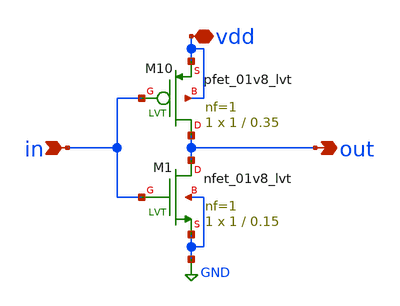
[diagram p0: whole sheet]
** sch_path: designs/subcells/core_not/not.sch
**.subckt not in out vdd
*.ipin in
*.opin out
*.iopin vdd
XM10 out in vdd vdd sky130_fd_pr__pfet_01v8_lvt L=0.35 W=1 nf=1 ad='int((1 + 1)/2) * 1 / 1 * 0.29' as='int((1 + 2)/2) * 1 / 1 * 0.29'
+ pd='2*int((1 + 1)/2) * (1 / 1 + 0.29)' ps='2*int((1 + 2)/2) * (1 / 1 + 0.29)' nrd='0.29 / 1 ' nrs='0.29 / 1 '
+ sa=0 sb=0 sd=0 mult=1 m=1
XM1 out in GND GND sky130_fd_pr__nfet_01v8_lvt L=0.15 W=1 nf=1 ad='int((1 + 1)/2) * 1 / 1 * 0.29' as='int((1 + 2)/2) * 1 / 1 * 0.29'
+ pd='2*int((1 + 1)/2) * (1 / 1 + 0.29)' ps='2*int((1 + 2)/2) * (1 / 1 + 0.29)' nrd='0.29 / 1 ' nrs='0.29 / 1 '
+ sa=0 sb=0 sd=0 mult=1 m=1
**.ends
.GLOBAL GND
.end
